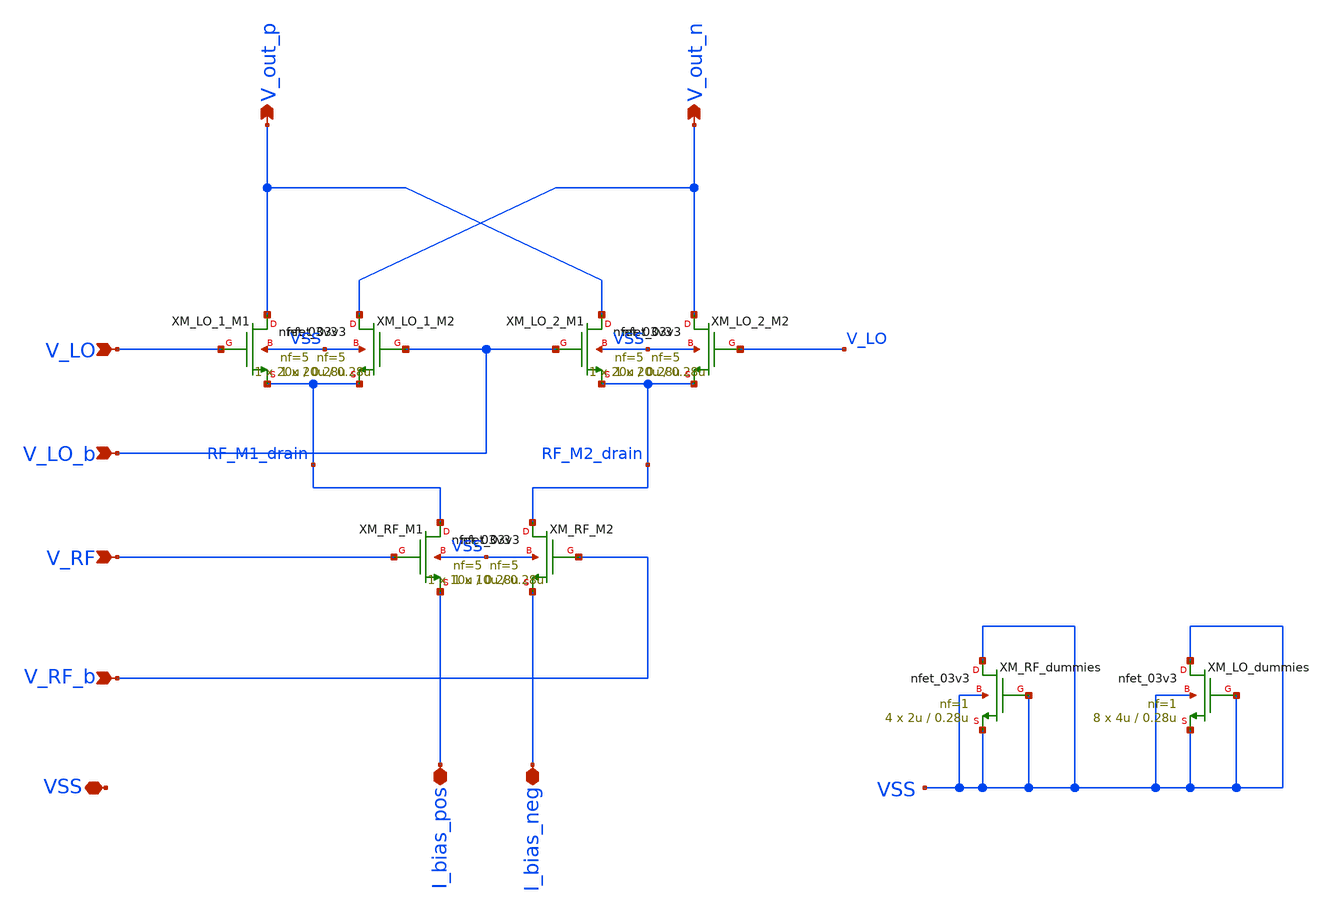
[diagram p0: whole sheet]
** sch_path: src/python/Gilbert_mixer/Gilbert_cell_hierarchal_mixing_stage.sch
**.subckt Gilbert_cell_hierarchal_mixing_stage V_LO V_LO_b V_RF V_RF_b V_out_p V_out_n I_bias_neg
*+ I_bias_pos VSS
*.ipin V_LO
*.ipin V_LO_b
*.ipin V_RF
*.ipin V_RF_b
*.opin V_out_p
*.opin V_out_n
*.iopin I_bias_neg
*.iopin I_bias_pos
*.iopin VSS
XM_LO_1_M1 V_out_p V_LO RF_M1_drain VSS nfet_03v3 L=0.28u W=20u nf=5 ad='int((nf+1)/2) * W/nf * 0.18u'
+ as='int((nf+2)/2) * W/nf * 0.18u' pd='2*int((nf+1)/2) * (W/nf + 0.18u)' ps='2*int((nf+2)/2) * (W/nf + 0.18u)'
+ nrd='0.18u / W' nrs='0.18u / W' sa=0 sb=0 sd=0 m=1
XM_LO_1_M2 V_out_n V_LO_b RF_M1_drain VSS nfet_03v3 L=0.28u W=20u nf=5 ad='int((nf+1)/2) * W/nf * 0.18u'
+ as='int((nf+2)/2) * W/nf * 0.18u' pd='2*int((nf+1)/2) * (W/nf + 0.18u)' ps='2*int((nf+2)/2) * (W/nf + 0.18u)'
+ nrd='0.18u / W' nrs='0.18u / W' sa=0 sb=0 sd=0 m=1
XM_LO_2_M1 V_out_p V_LO_b RF_M2_drain VSS nfet_03v3 L=0.28u W=20u nf=5 ad='int((nf+1)/2) * W/nf * 0.18u'
+ as='int((nf+2)/2) * W/nf * 0.18u' pd='2*int((nf+1)/2) * (W/nf + 0.18u)' ps='2*int((nf+2)/2) * (W/nf + 0.18u)'
+ nrd='0.18u / W' nrs='0.18u / W' sa=0 sb=0 sd=0 m=1
XM_LO_2_M2 V_out_n V_LO RF_M2_drain VSS nfet_03v3 L=0.28u W=20u nf=5 ad='int((nf+1)/2) * W/nf * 0.18u'
+ as='int((nf+2)/2) * W/nf * 0.18u' pd='2*int((nf+1)/2) * (W/nf + 0.18u)' ps='2*int((nf+2)/2) * (W/nf + 0.18u)'
+ nrd='0.18u / W' nrs='0.18u / W' sa=0 sb=0 sd=0 m=1
XM_RF_M1 RF_M1_drain V_RF I_bias_pos VSS nfet_03v3 L=0.28u W=10u nf=5 ad='int((nf+1)/2) * W/nf * 0.18u'
+ as='int((nf+2)/2) * W/nf * 0.18u' pd='2*int((nf+1)/2) * (W/nf + 0.18u)' ps='2*int((nf+2)/2) * (W/nf + 0.18u)'
+ nrd='0.18u / W' nrs='0.18u / W' sa=0 sb=0 sd=0 m=1
XM_RF_M2 RF_M2_drain V_RF_b I_bias_neg VSS nfet_03v3 L=0.28u W=10u nf=5 ad='int((nf+1)/2) * W/nf * 0.18u'
+ as='int((nf+2)/2) * W/nf * 0.18u' pd='2*int((nf+1)/2) * (W/nf + 0.18u)' ps='2*int((nf+2)/2) * (W/nf + 0.18u)'
+ nrd='0.18u / W' nrs='0.18u / W' sa=0 sb=0 sd=0 m=1
XM_RF_dummies VSS VSS VSS VSS nfet_03v3 L=0.28u W=2u nf=1 ad='int((nf+1)/2) * W/nf * 0.18u' as='int((nf+2)/2) * W/nf * 0.18u'
+ pd='2*int((nf+1)/2) * (W/nf + 0.18u)' ps='2*int((nf+2)/2) * (W/nf + 0.18u)' nrd='0.18u / W' nrs='0.18u / W'
+ sa=0 sb=0 sd=0 m=4
XM_LO_dummies VSS VSS VSS VSS nfet_03v3 L=0.28u W=4u nf=1 ad='int((nf+1)/2) * W/nf * 0.18u' as='int((nf+2)/2) * W/nf * 0.18u'
+ pd='2*int((nf+1)/2) * (W/nf + 0.18u)' ps='2*int((nf+2)/2) * (W/nf + 0.18u)' nrd='0.18u / W' nrs='0.18u / W'
+ sa=0 sb=0 sd=0 m=8
**.ends
.end
